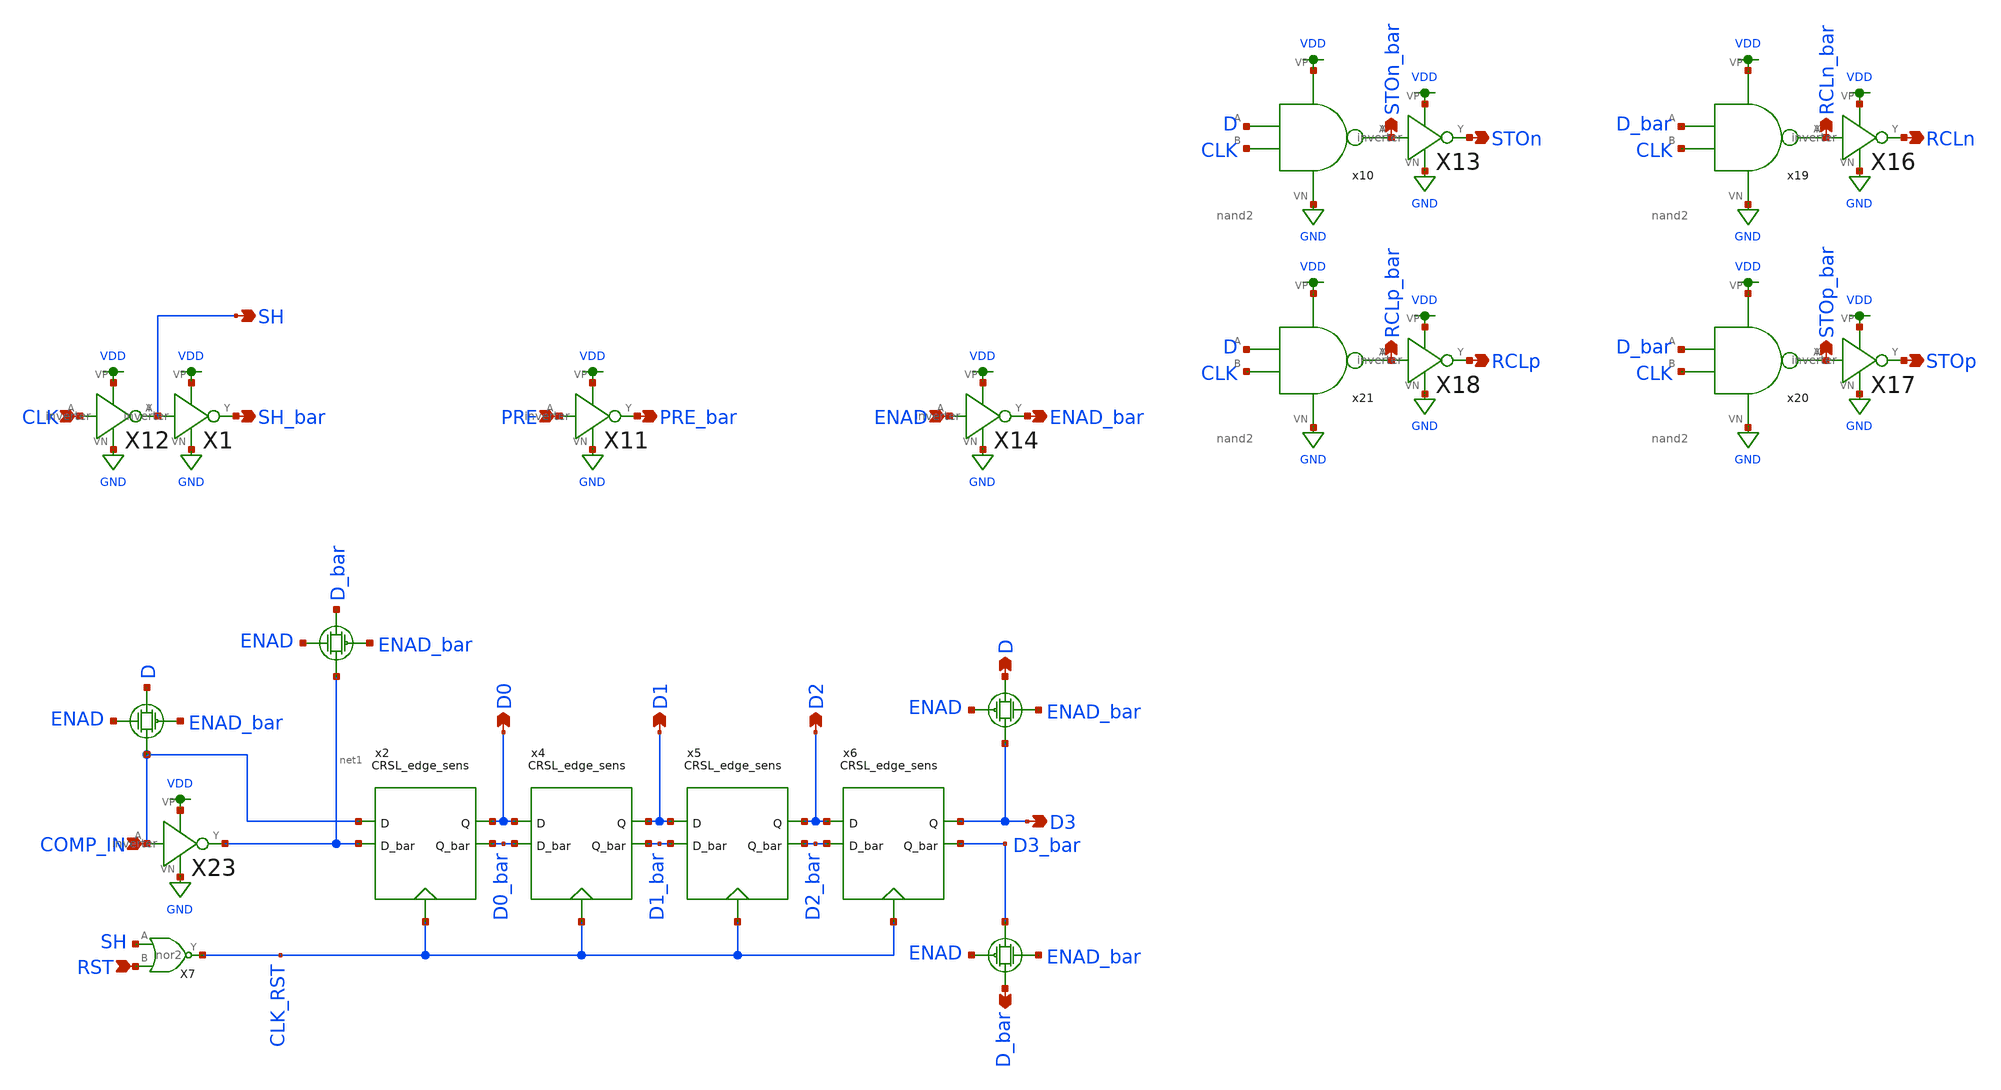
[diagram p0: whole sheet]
** sch_path: schematics/digital_control.sch
**.subckt digital_control COMP_IN D1 D2 D0 CLK SH_bar SH PRE PRE_bar ENAD ENAD_bar STOp STOn RCLp
*+ RCLn STOn_bar STOp_bar RCLn_bar RCLp_bar RST D3 D D_bar
*.ipin COMP_IN
*.opin D1
*.opin D2
*.opin D0
*.ipin CLK
*.opin SH_bar
*.opin SH
*.ipin PRE
*.opin PRE_bar
*.ipin ENAD
*.opin ENAD_bar
*.opin STOp
*.opin STOn
*.opin RCLp
*.opin RCLn
*.opin STOn_bar
*.opin STOp_bar
*.opin RCLn_bar
*.opin RCLp_bar
*.ipin RST
*.opin D3
*.opin D
*.opin D_bar
x4 CLK_RST D1 D0 D1_bar D0_bar CRSL_edge_sens
x5 CLK_RST D2 D1 D2_bar D1_bar CRSL_edge_sens
x6 CLK_RST D3 D2 D3_bar D2_bar CRSL_edge_sens
x10 VDD CLK STOn_bar D GND nand2
X13 STOn_bar STOn VDD GND inverter
X16 RCLn_bar RCLn VDD GND inverter
X17 STOp_bar STOp VDD GND inverter
X18 RCLp_bar RCLp VDD GND inverter
x19 VDD CLK RCLn_bar D_bar GND nand2
x20 VDD CLK STOp_bar D_bar GND nand2
x21 VDD CLK RCLp_bar D GND nand2
X23 COMP_IN net1 VDD GND inverter
X12 CLK SH VDD GND inverter
X1 SH SH_bar VDD GND inverter
X11 PRE PRE_bar VDD GND inverter
X14 ENAD ENAD_bar VDD GND inverter
x2 CLK_RST D0 COMP_IN D0_bar net1 CRSL_edge_sens
X7 SH CLK_RST RST nor2
**.ends

* expanding   symbol:  ../schematics/CRSL_edge_sens.sym # of pins=5
** sym_path: schematics/CRSL_edge_sens.sym
** sch_path: schematics/CRSL_edge_sens.sch
.subckt CRSL_edge_sens Phi Q D Q_bar D_bar
*.ipin D
*.ipin D_bar
*.opin Q
*.opin Q_bar
*.ipin Phi
XM14 Q_bar Q GND GND sky130_fd_pr__nfet_01v8 L=0.15 W=1 nf=1 ad='int((nf+1)/2) * W/nf * 0.29' as='int((nf+2)/2) * W/nf * 0.29'
+ pd='2*int((nf+1)/2) * (W/nf + 0.29)' ps='2*int((nf+2)/2) * (W/nf + 0.29)' nrd='0.29 / W' nrs='0.29 / W'
+ sa=0 sb=0 sd=0 mult=1 m=1
XM2 Q_bar Phi net3 GND sky130_fd_pr__nfet_01v8 L=0.15 W=1 nf=1 ad='int((nf+1)/2) * W/nf * 0.29' as='int((nf+2)/2) * W/nf * 0.29'
+ pd='2*int((nf+1)/2) * (W/nf + 0.29)' ps='2*int((nf+2)/2) * (W/nf + 0.29)' nrd='0.29 / W' nrs='0.29 / W'
+ sa=0 sb=0 sd=0 mult=1 m=1
XM6 Q Phi net2 GND sky130_fd_pr__nfet_01v8 L=0.15 W=1 nf=1 ad='int((nf+1)/2) * W/nf * 0.29' as='int((nf+2)/2) * W/nf * 0.29'
+ pd='2*int((nf+1)/2) * (W/nf + 0.29)' ps='2*int((nf+2)/2) * (W/nf + 0.29)' nrd='0.29 / W' nrs='0.29 / W'
+ sa=0 sb=0 sd=0 mult=1 m=1
XM7 net4 Phi GND GND sky130_fd_pr__nfet_01v8 L=0.15 W=4 nf=1 ad='int((nf+1)/2) * W/nf * 0.29' as='int((nf+2)/2) * W/nf * 0.29'
+ pd='2*int((nf+1)/2) * (W/nf + 0.29)' ps='2*int((nf+2)/2) * (W/nf + 0.29)' nrd='0.29 / W' nrs='0.29 / W'
+ sa=0 sb=0 sd=0 mult=1 m=1
XM8 net3 net2 net4 GND sky130_fd_pr__nfet_01v8 L=0.15 W=1 nf=1 ad='int((nf+1)/2) * W/nf * 0.29' as='int((nf+2)/2) * W/nf * 0.29'
+ pd='2*int((nf+1)/2) * (W/nf + 0.29)' ps='2*int((nf+2)/2) * (W/nf + 0.29)' nrd='0.29 / W' nrs='0.29 / W'
+ sa=0 sb=0 sd=0 mult=1 m=1
XM12 net3 net2 VDD VDD sky130_fd_pr__pfet_01v8 L=0.15 W=1 nf=1 ad='int((nf+1)/2) * W/nf * 0.29' as='int((nf+2)/2) * W/nf * 0.29'
+ pd='2*int((nf+1)/2) * (W/nf + 0.29)' ps='2*int((nf+2)/2) * (W/nf + 0.29)' nrd='0.29 / W' nrs='0.29 / W'
+ sa=0 sb=0 sd=0 mult=1 m=1
XM9 net2 net3 VDD VDD sky130_fd_pr__pfet_01v8 L=0.15 W=1 nf=1 ad='int((nf+1)/2) * W/nf * 0.29' as='int((nf+2)/2) * W/nf * 0.29'
+ pd='2*int((nf+1)/2) * (W/nf + 0.29)' ps='2*int((nf+2)/2) * (W/nf + 0.29)' nrd='0.29 / W' nrs='0.29 / W'
+ sa=0 sb=0 sd=0 mult=1 m=1
XM1 net1 Phi VDD VDD sky130_fd_pr__pfet_01v8 L=0.15 W=4 nf=1 ad='int((nf+1)/2) * W/nf * 0.29' as='int((nf+2)/2) * W/nf * 0.29'
+ pd='2*int((nf+1)/2) * (W/nf + 0.29)' ps='2*int((nf+2)/2) * (W/nf + 0.29)' nrd='0.29 / W' nrs='0.29 / W'
+ sa=0 sb=0 sd=0 mult=1 m=1
XM3 Q_bar Q net1 VDD sky130_fd_pr__pfet_01v8 L=0.15 W=1 nf=1 ad='int((nf+1)/2) * W/nf * 0.29' as='int((nf+2)/2) * W/nf * 0.29'
+ pd='2*int((nf+1)/2) * (W/nf + 0.29)' ps='2*int((nf+2)/2) * (W/nf + 0.29)' nrd='0.29 / W' nrs='0.29 / W'
+ sa=0 sb=0 sd=0 mult=1 m=1
XM4 Q Q_bar net1 VDD sky130_fd_pr__pfet_01v8 L=0.15 W=1 nf=1 ad='int((nf+1)/2) * W/nf * 0.29' as='int((nf+2)/2) * W/nf * 0.29'
+ pd='2*int((nf+1)/2) * (W/nf + 0.29)' ps='2*int((nf+2)/2) * (W/nf + 0.29)' nrd='0.29 / W' nrs='0.29 / W'
+ sa=0 sb=0 sd=0 mult=1 m=1
XM10 Q Q_bar GND GND sky130_fd_pr__nfet_01v8 L=0.15 W=1 nf=1 ad='int((nf+1)/2) * W/nf * 0.29' as='int((nf+2)/2) * W/nf * 0.29'
+ pd='2*int((nf+1)/2) * (W/nf + 0.29)' ps='2*int((nf+2)/2) * (W/nf + 0.29)' nrd='0.29 / W' nrs='0.29 / W'
+ sa=0 sb=0 sd=0 mult=1 m=1
XM5 net2 net3 net4 GND sky130_fd_pr__nfet_01v8 L=0.15 W=1 nf=1 ad='int((nf+1)/2) * W/nf * 0.29' as='int((nf+2)/2) * W/nf * 0.29'
+ pd='2*int((nf+1)/2) * (W/nf + 0.29)' ps='2*int((nf+2)/2) * (W/nf + 0.29)' nrd='0.29 / W' nrs='0.29 / W'
+ sa=0 sb=0 sd=0 mult=1 m=1
XM11 net3 Phi D_bar VDD sky130_fd_pr__pfet_01v8 L=0.15 W=1 nf=1 ad='int((nf+1)/2) * W/nf * 0.29' as='int((nf+2)/2) * W/nf * 0.29'
+ pd='2*int((nf+1)/2) * (W/nf + 0.29)' ps='2*int((nf+2)/2) * (W/nf + 0.29)' nrd='0.29 / W' nrs='0.29 / W'
+ sa=0 sb=0 sd=0 mult=1 m=1
XM15 net2 Phi D VDD sky130_fd_pr__pfet_01v8 L=0.15 W=1 nf=1 ad='int((nf+1)/2) * W/nf * 0.29' as='int((nf+2)/2) * W/nf * 0.29'
+ pd='2*int((nf+1)/2) * (W/nf + 0.29)' ps='2*int((nf+2)/2) * (W/nf + 0.29)' nrd='0.29 / W' nrs='0.29 / W'
+ sa=0 sb=0 sd=0 mult=1 m=1
.ends


* expanding   symbol:  ../schematics/nand2.sym # of pins=5
** sym_path: schematics/nand2.sym
** sch_path: schematics/nand2.sch
.subckt nand2 VP B Y A VN
*.iopin VP
*.iopin VN
*.ipin A
*.ipin B
*.opin Y
XM5 Y B VP VP sky130_fd_pr__pfet_01v8 L=0.15 W=1 nf=1 ad='int((nf+1)/2) * W/nf * 0.29' as='int((nf+2)/2) * W/nf * 0.29'
+ pd='2*int((nf+1)/2) * (W/nf + 0.29)' ps='2*int((nf+2)/2) * (W/nf + 0.29)' nrd='0.29 / W' nrs='0.29 / W'
+ sa=0 sb=0 sd=0 mult=1 m=1
XM2 Y A VP VP sky130_fd_pr__pfet_01v8 L=0.15 W=1 nf=1 ad='int((nf+1)/2) * W/nf * 0.29' as='int((nf+2)/2) * W/nf * 0.29'
+ pd='2*int((nf+1)/2) * (W/nf + 0.29)' ps='2*int((nf+2)/2) * (W/nf + 0.29)' nrd='0.29 / W' nrs='0.29 / W'
+ sa=0 sb=0 sd=0 mult=1 m=1
XM1 Y A net1 VN sky130_fd_pr__nfet_01v8 L=0.15 W=1 nf=1 ad='int((nf+1)/2) * W/nf * 0.29' as='int((nf+2)/2) * W/nf * 0.29'
+ pd='2*int((nf+1)/2) * (W/nf + 0.29)' ps='2*int((nf+2)/2) * (W/nf + 0.29)' nrd='0.29 / W' nrs='0.29 / W'
+ sa=0 sb=0 sd=0 mult=1 m=1
XM3 net1 B VN VN sky130_fd_pr__nfet_01v8 L=0.15 W=1 nf=1 ad='int((nf+1)/2) * W/nf * 0.29' as='int((nf+2)/2) * W/nf * 0.29'
+ pd='2*int((nf+1)/2) * (W/nf + 0.29)' ps='2*int((nf+2)/2) * (W/nf + 0.29)' nrd='0.29 / W' nrs='0.29 / W'
+ sa=0 sb=0 sd=0 mult=1 m=1
.ends


* expanding   symbol:  ../schematics/inverter.sym # of pins=4
** sym_path: schematics/inverter.sym
** sch_path: schematics/inverter.sch
.subckt inverter A Y VP VN
*.ipin A
*.iopin VP
*.iopin VN
*.opin Y
XM1 Y A VP VDD sky130_fd_pr__pfet_01v8 L=0.15 W=1 nf=1 ad='int((nf+1)/2) * W/nf * 0.29' as='int((nf+2)/2) * W/nf * 0.29'
+ pd='2*int((nf+1)/2) * (W/nf + 0.29)' ps='2*int((nf+2)/2) * (W/nf + 0.29)' nrd='0.29 / W' nrs='0.29 / W'
+ sa=0 sb=0 sd=0 mult=1 m=1
XM2 Y A VN GND sky130_fd_pr__nfet_01v8 L=0.15 W=1 nf=1 ad='int((nf+1)/2) * W/nf * 0.29' as='int((nf+2)/2) * W/nf * 0.29'
+ pd='2*int((nf+1)/2) * (W/nf + 0.29)' ps='2*int((nf+2)/2) * (W/nf + 0.29)' nrd='0.29 / W' nrs='0.29 / W'
+ sa=0 sb=0 sd=0 mult=1 m=1
.ends


* expanding   symbol:  /home/madvlsi/Documents/algorithmic-ada-converter/schematics/nor2.sym # of
*+ pins=3
** sym_path: schematics/nor2.sym
** sch_path: schematics/nor2.sch
.subckt nor2 A Y B
*.ipin A
*.ipin B
*.opin Y
XM4 Y B GND GND sky130_fd_pr__nfet_01v8 L=0.15 W=1 nf=1 ad='int((nf+1)/2) * W/nf * 0.29' as='int((nf+2)/2) * W/nf * 0.29'
+ pd='2*int((nf+1)/2) * (W/nf + 0.29)' ps='2*int((nf+2)/2) * (W/nf + 0.29)' nrd='0.29 / W' nrs='0.29 / W'
+ sa=0 sb=0 sd=0 mult=1 m=1
XM6 Y A GND GND sky130_fd_pr__nfet_01v8 L=0.15 W=1 nf=1 ad='int((nf+1)/2) * W/nf * 0.29' as='int((nf+2)/2) * W/nf * 0.29'
+ pd='2*int((nf+1)/2) * (W/nf + 0.29)' ps='2*int((nf+2)/2) * (W/nf + 0.29)' nrd='0.29 / W' nrs='0.29 / W'
+ sa=0 sb=0 sd=0 mult=1 m=1
XM7 Y B net1 VDD sky130_fd_pr__pfet_01v8 L=0.15 W=1 nf=1 ad='int((nf+1)/2) * W/nf * 0.29' as='int((nf+2)/2) * W/nf * 0.29'
+ pd='2*int((nf+1)/2) * (W/nf + 0.29)' ps='2*int((nf+2)/2) * (W/nf + 0.29)' nrd='0.29 / W' nrs='0.29 / W'
+ sa=0 sb=0 sd=0 mult=1 m=1
XM8 net1 A VDD VDD sky130_fd_pr__pfet_01v8 L=0.15 W=1 nf=1 ad='int((nf+1)/2) * W/nf * 0.29' as='int((nf+2)/2) * W/nf * 0.29'
+ pd='2*int((nf+1)/2) * (W/nf + 0.29)' ps='2*int((nf+2)/2) * (W/nf + 0.29)' nrd='0.29 / W' nrs='0.29 / W'
+ sa=0 sb=0 sd=0 mult=1 m=1
.ends

.GLOBAL GND
.GLOBAL VDD
.end
